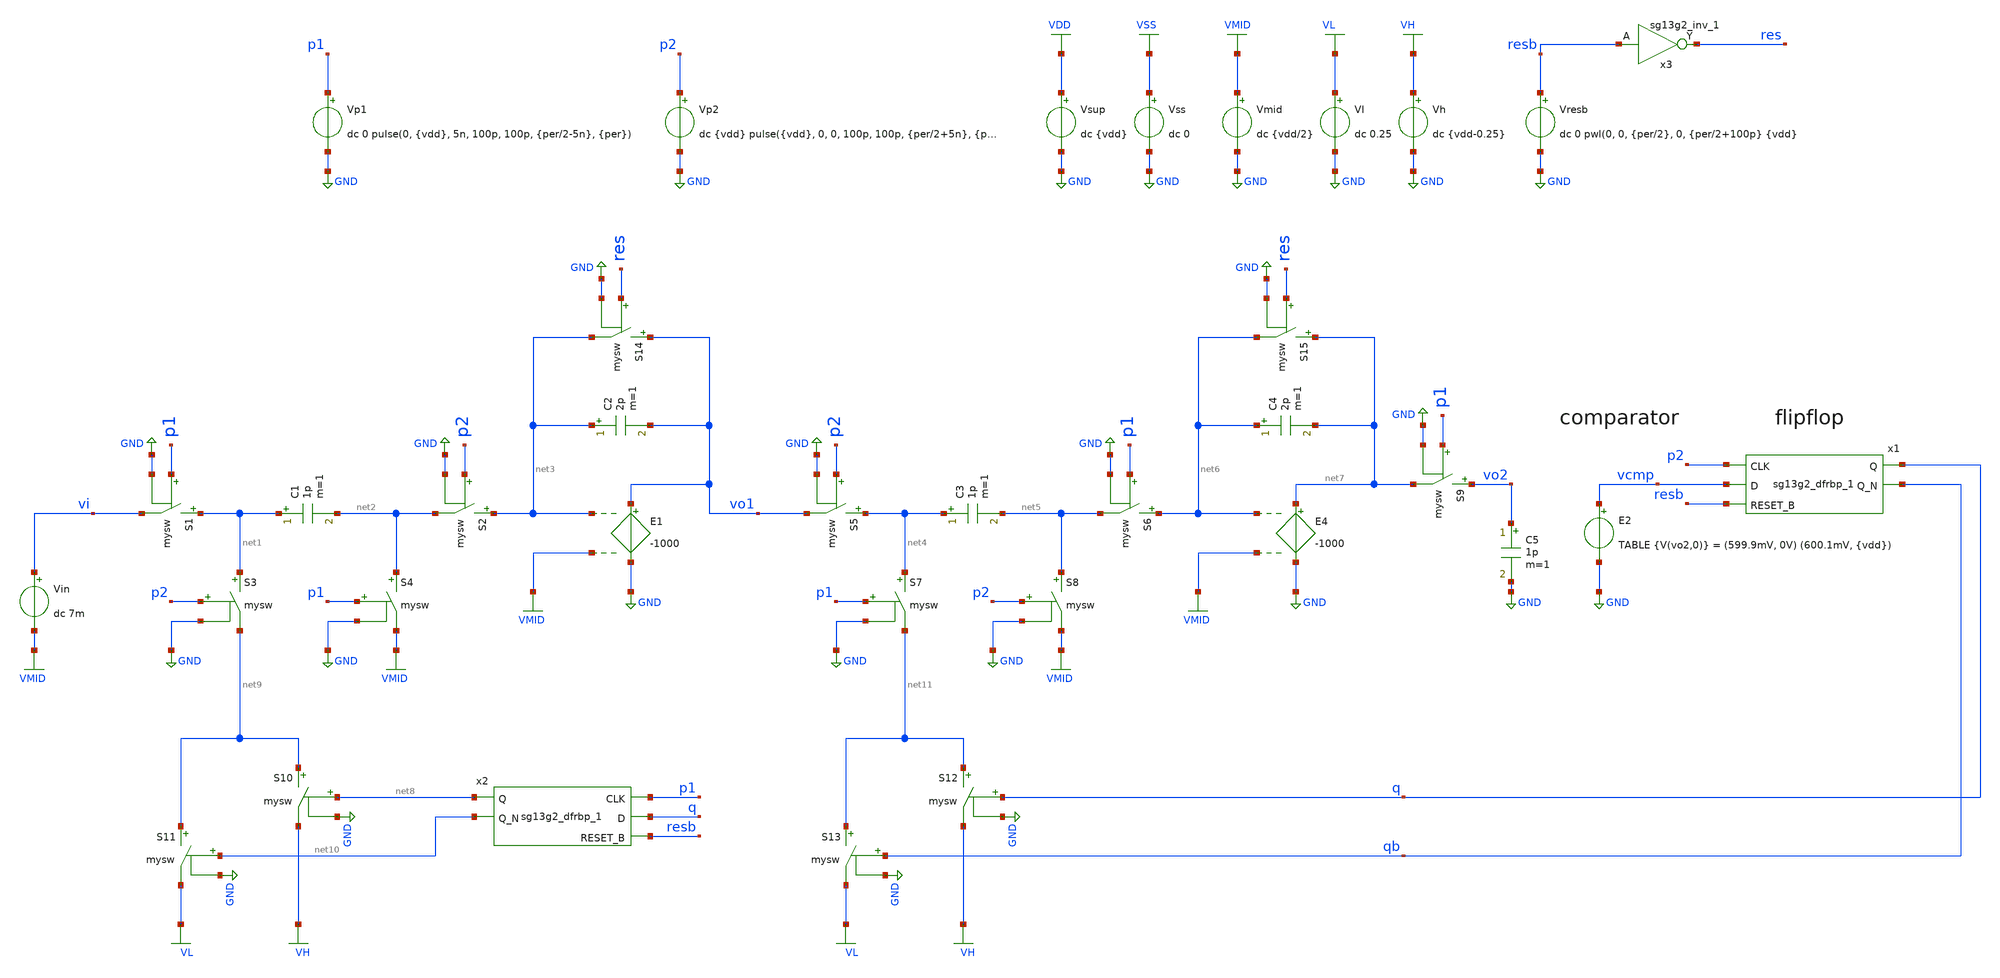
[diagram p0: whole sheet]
** sch_path: 5_Design/2_Idealized_circuits/tb_ideal_idsm2_scaled.sch
**.subckt tb_ideal_idsm2_scaled
Vp1 p1 GND dc 0 pulse(0, {vdd}, 5n, 100p, 100p, {per/2-5n}, {per})
E1 vo1 GND net3 VMID -1000
S1 net1 vi p1 GND mysw
Vp2 p2 GND dc {vdd} pulse({vdd}, 0, 0, 100p, 100p, {per/2+5n}, {per})
Vin vi VMID dc 7m
C1 net1 net2 1p m=1
S2 net3 net2 p2 GND mysw
C2 net3 vo1 2p m=1
S3 net1 net9 p2 GND mysw
S4 net2 VMID p1 GND mysw
E2 vcmp GND TABLE {V(vo2,0)} = (599.9mV, 0V) (600.1mV, {vdd})
Vsup VDD GND dc {vdd}
Vresb resb GND dc 0 pwl(0, 0, {per/2}, 0, {per/2+100p} {vdd}
x1 q qb p2 vcmp resb VDD VSS sg13g2_dfrbp_1
Vss VSS GND dc 0
E4 net7 GND net6 VMID -1000
S5 net4 vo1 p2 GND mysw
C3 net4 net5 1p m=1
S6 net6 net5 p1 GND mysw
C4 net6 net7 2p m=1
S7 net4 net11 p1 GND mysw
S8 net5 VMID p2 GND mysw
S9 vo2 net7 p1 GND mysw
C5 vo2 GND 1p m=1
x2 net8 net10 p1 q resb VDD VSS sg13g2_dfrbp_1
Vmid VMID GND dc {vdd/2}
S10 net9 VH net8 GND mysw
S11 net9 VL net10 GND mysw
S12 net11 VH q GND mysw
S13 net11 VL qb GND mysw
Vl VL GND dc 0.25
Vh VH GND dc {vdd-0.25}
S14 vo1 net3 res GND mysw
S15 net7 net6 res GND mysw
x3 res resb VDD VSS sg13g2_inv_1
**** begin user architecture code

.lib $::SG13G2_MODELS/cornerMOSlv.lib mos_tt
.lib $::SG13G2_MODELS/cornerRES.lib res_typ
.inc /foss/pdks/sg13g2/libs.ref/sg13g2_stdcell/spice/sg13g2_stdcell.spice



.param temp=27 vdd=1.2 per=1u
.model mysw SW vt={vdd/2} ron=10k roff=1gig
.option method=gear reltol=1e-4

.control
save all
tran 1n 65u
plot vo1 vo2 q
set wr_singlescale
set wr_vecnames
wrdata tb_ideal_idsm2_scaled.txt vo1 vo2 q p1 p2
.endc


**** end user architecture code
**.ends

* expanding   symbol:  sg13g2_stdcells/sg13g2_dfrbp_1.sym # of pins=5
** sym_path: sg13g2_stdcells/sg13g2_dfrbp_1.sym
** sch_path: sg13g2_stdcells/sg13g2_dfrbp_1.sch
.subckt sg13g2_dfrbp_1 Q Q_N CLK D RESET_B VDD VSS
*.ipin D
*.ipin RESET_B
*.ipin CLK
*.opin Q
*.opin Q_N
*.iopin VDD
*.iopin VSS
XM1 Db D net10 VSS sg13_lv_nmos w=420.00n l=130.00n ng=1 m=1 mm_ok=1
XM2 net10 RESET_B VSS VSS sg13_lv_nmos w=420.00n l=130.00n ng=1 m=1 mm_ok=1
XM3 net1 clkneg net9 VSS sg13_lv_nmos w=420.00n l=130.00n ng=1 m=1 mm_ok=1
XM4 net9 net1 VSS VSS sg13_lv_nmos w=420.00n l=130.00n ng=1 m=1 mm_ok=1
XM5 net1 net1 net5 VSS sg13_lv_nmos w=420.00n l=130.00n ng=1 m=1 mm_ok=1
XM6 net5 RESET_B VSS VSS sg13_lv_nmos w=420.00n l=130.00n ng=1 m=1 mm_ok=1
XM7 Q_N net1 VSS VSS sg13_lv_nmos w=740.00n l=130.00n ng=1 m=1 mm_ok=1
XM8 net2 net1 VSS VSS sg13_lv_nmos w=740.00n l=130.00n ng=1 m=1 mm_ok=1
XM9 Q net2 VSS VSS sg13_lv_nmos w=740.00n l=130.00n ng=1 m=1 mm_ok=1
XM10 clkneg CLK VSS VSS sg13_lv_nmos w=740.00n l=130.00n ng=1 m=1 mm_ok=1
XM11 clkpos clkneg VSS VSS sg13_lv_nmos w=740.00n l=130.00n ng=1 m=1 mm_ok=1
XM12 Db clkneg net3 VSS sg13_lv_nmos w=420.00n l=130.00n ng=1 m=1 mm_ok=1
XM13 net3 clkpos net8 VSS sg13_lv_nmos w=420.00n l=130.00n ng=1 m=1 mm_ok=1
XM14 net8 net3 net4 VSS sg13_lv_nmos w=420.00n l=130.00n ng=1 m=1 mm_ok=1
XM15 net4 RESET_B VSS VSS sg13_lv_nmos w=420.00n l=130.00n ng=1 m=1 mm_ok=1
XM16 net3 net3 VSS VSS sg13_lv_nmos w=740.00n l=130.00n ng=1 m=1 mm_ok=1
XM17 net3 clkpos net1 VSS sg13_lv_nmos w=740.00n l=130.00n ng=1 m=1 mm_ok=1
XM18 Db RESET_B VDD VDD sg13_lv_pmos w=420.00n l=130.00n ng=1 m=1 mm_ok=1
XM19 Db D VDD VDD sg13_lv_pmos w=420.00n l=130.00n ng=1 m=1 mm_ok=1
XM20 net7 net1 VDD VDD sg13_lv_pmos w=420.00n l=130.00n ng=1 m=1 mm_ok=1
XM21 net1 clkpos net7 VDD sg13_lv_pmos w=420.00n l=130.00n ng=1 m=1 mm_ok=1
XM22 net1 net1 VDD VDD sg13_lv_pmos w=420.00n l=130.00n ng=1 m=1 mm_ok=1
XM23 net1 RESET_B VDD VDD sg13_lv_pmos w=420.00n l=130.00n ng=1 m=1 mm_ok=1
XM24 Q_N net1 VDD VDD sg13_lv_pmos w=1.12u l=130.00n ng=1 m=1 mm_ok=1
XM25 net2 net1 VDD VDD sg13_lv_pmos w=1.12u l=130.00n ng=1 m=1 mm_ok=1
XM26 Q net2 VDD VDD sg13_lv_pmos w=1.12u l=130.00n ng=1 m=1 mm_ok=1
XM27 clkneg CLK VDD VDD sg13_lv_pmos w=1.12u l=130.00n ng=1 m=1 mm_ok=1
XM28 clkpos clkneg VDD VDD sg13_lv_pmos w=1.12u l=130.00n ng=1 m=1 mm_ok=1
XM29 Db clkpos net3 VDD sg13_lv_pmos w=420.00n l=130.00n ng=1 m=1 mm_ok=1
XM30 net6 net3 VDD VDD sg13_lv_pmos w=420.00n l=130.00n ng=1 m=1 mm_ok=1
XM31 net3 clkneg net6 VDD sg13_lv_pmos w=420.00n l=130.00n ng=1 m=1 mm_ok=1
XM32 net3 RESET_B VDD VDD sg13_lv_pmos w=420.00n l=130.00n ng=1 m=1 mm_ok=1
XM33 net3 net3 VDD VDD sg13_lv_pmos w=1.000u l=130.00n ng=1 m=1 mm_ok=1
XM34 net3 clkneg net1 VDD sg13_lv_pmos w=1.000u l=130.00n ng=1 m=1 mm_ok=1
.ends


* expanding   symbol:  sg13g2_stdcells/sg13g2_inv_1.sym # of pins=2
** sym_path: sg13g2_stdcells/sg13g2_inv_1.sym
** sch_path: sg13g2_stdcells/sg13g2_inv_1.sch
.subckt sg13g2_inv_1 Y A VDD VSS
*.opin Y
*.ipin A
*.iopin VDD
*.iopin VSS
XM1 Y A VSS VSS sg13_lv_nmos w=740.00n l=130.00n ng=1 m=1 mm_ok=1
XM2 Y A VDD VDD sg13_lv_pmos w=1.12u l=130.00n ng=1 m=1 mm_ok=1
.ends

.GLOBAL GND
.GLOBAL VDD
.GLOBAL VSS
.GLOBAL VMID
.GLOBAL VL
.GLOBAL VH
.end
